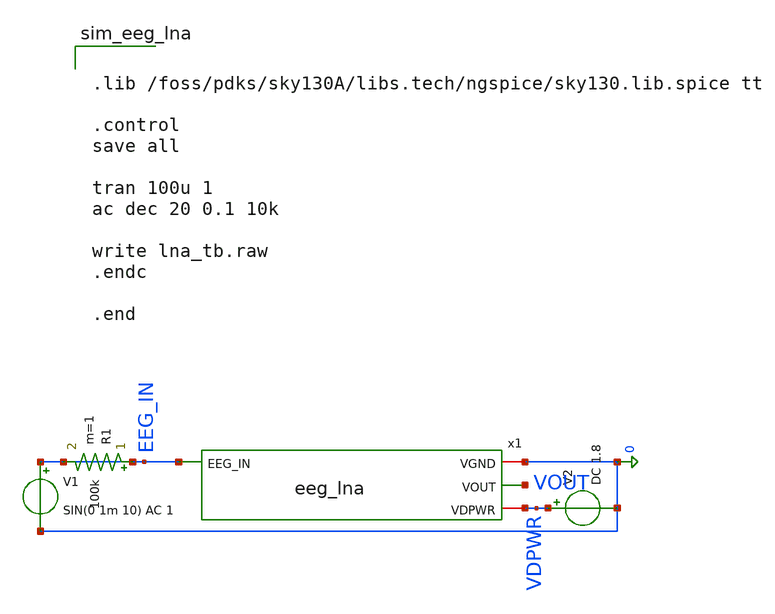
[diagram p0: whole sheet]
** sch_path: xschem/eeg_lna_tb.sch
**.subckt eeg_lna_tb
V1 EEG_IN 0 SIN(0 1m 10) AC 1
V2 VDPWR 0 DC 1.8
x1 EEG_IN 0 VOUT VDPWR eeg_lna
R1 EEG_IN EEG_IN 100k m=1
**** begin user architecture code


.lib /foss/pdks/sky130A/libs.tech/ngspice/sky130.lib.spice tt

.control
save all

tran 100u 1
ac dec 20 0.1 10k

write lna_tb.raw
.endc

.end


**** end user architecture code
**.ends

* expanding   symbol:  eeg_lna.sym # of pins=4
** sym_path: xschem/eeg_lna.sym
** sch_path: xschem/eeg_lna.sch
.subckt eeg_lna EEG_IN VGND VOUT VDPWR
*.iopin VGND
*.ipin EEG_IN
*.iopin VDPWR
*.opin VOUT
XM1 MIRROR_BIAS_N MIRROR_BIAS_N VGND VGND sky130_fd_pr__nfet_01v8 L=1.0 W=4 nf=1 ad='int((1 + 1)/2) * 4 / 1 * 0.29'
+ as='int((1 + 2)/2) * 4 / 1 * 0.29' pd='2*int((1 + 1)/2) * (4 / 1 + 0.29)' ps='2*int((1 + 2)/2) * (4 / 1 + 0.29)'
+ nrd='0.29 / 4 ' nrs='0.29 / 4 ' sa=0 sb=0 sd=0 mult=1 m=1
XM2 VOUT MIRROR_BIAS_N VGND VGND sky130_fd_pr__nfet_01v8 L=1.0 W=4 nf=1 ad='int((1 + 1)/2) * 4 / 1 * 0.29'
+ as='int((1 + 2)/2) * 4 / 1 * 0.29' pd='2*int((1 + 1)/2) * (4 / 1 + 0.29)' ps='2*int((1 + 2)/2) * (4 / 1 + 0.29)'
+ nrd='0.29 / 4 ' nrs='0.29 / 4 ' sa=0 sb=0 sd=0 mult=1 m=1
XM3 MIRROR_BIAS_N VIN_P TAIL_P VDPWR sky130_fd_pr__pfet_01v8 L=1.0 W=8 nf=1 ad='int((1 + 1)/2) * 8 / 1 * 0.29'
+ as='int((1 + 2)/2) * 8 / 1 * 0.29' pd='2*int((1 + 1)/2) * (8 / 1 + 0.29)' ps='2*int((1 + 2)/2) * (8 / 1 + 0.29)'
+ nrd='0.29 / 8 ' nrs='0.29 / 8 ' sa=0 sb=0 sd=0 mult=1 m=1
XM4 VOUT VIN_N TAIL_P VDPWR sky130_fd_pr__pfet_01v8 L=1.0 W=8 nf=1 ad='int((1 + 1)/2) * 8 / 1 * 0.29'
+ as='int((1 + 2)/2) * 8 / 1 * 0.29' pd='2*int((1 + 1)/2) * (8 / 1 + 0.29)' ps='2*int((1 + 2)/2) * (8 / 1 + 0.29)'
+ nrd='0.29 / 8 ' nrs='0.29 / 8 ' sa=0 sb=0 sd=0 mult=1 m=1
XM5 TAIL_P BIAS_P VDPWR VDPWR sky130_fd_pr__pfet_01v8 L=1.0 W=8 nf=1 ad='int((1 + 1)/2) * 8 / 1 * 0.29'
+ as='int((1 + 2)/2) * 8 / 1 * 0.29' pd='2*int((1 + 1)/2) * (8 / 1 + 0.29)' ps='2*int((1 + 2)/2) * (8 / 1 + 0.29)'
+ nrd='0.29 / 8 ' nrs='0.29 / 8 ' sa=0 sb=0 sd=0 mult=1 m=1
XM6 BIAS_P BIAS_P VDPWR VDPWR sky130_fd_pr__pfet_01v8 L=1.0 W=4 nf=1 ad='int((1 + 1)/2) * 4 / 1 * 0.29'
+ as='int((1 + 2)/2) * 4 / 1 * 0.29' pd='2*int((1 + 1)/2) * (4 / 1 + 0.29)' ps='2*int((1 + 2)/2) * (4 / 1 + 0.29)'
+ nrd='0.29 / 4 ' nrs='0.29 / 4 ' sa=0 sb=0 sd=0 mult=1 m=1
XM7 BIAS_P BIAS_P VGND VGND sky130_fd_pr__nfet_01v8 L=1.0 W=2 nf=1 ad='int((1 + 1)/2) * 2 / 1 * 0.29'
+ as='int((1 + 2)/2) * 2 / 1 * 0.29' pd='2*int((1 + 1)/2) * (2 / 1 + 0.29)' ps='2*int((1 + 2)/2) * (2 / 1 + 0.29)'
+ nrd='0.29 / 2 ' nrs='0.29 / 2 ' sa=0 sb=0 sd=0 mult=1 m=1
XCIN VIN_P EEG_IN sky130_fd_pr__cap_mim_m3_1 W=20 L=20 MF=1 m=1
RBIAS VIN_P BIAS_P 1Gig m=1
RF VOUT VIN_N 1Meg m=1
RG VIN_N BIAS_P 100k m=1
.ends

.end
